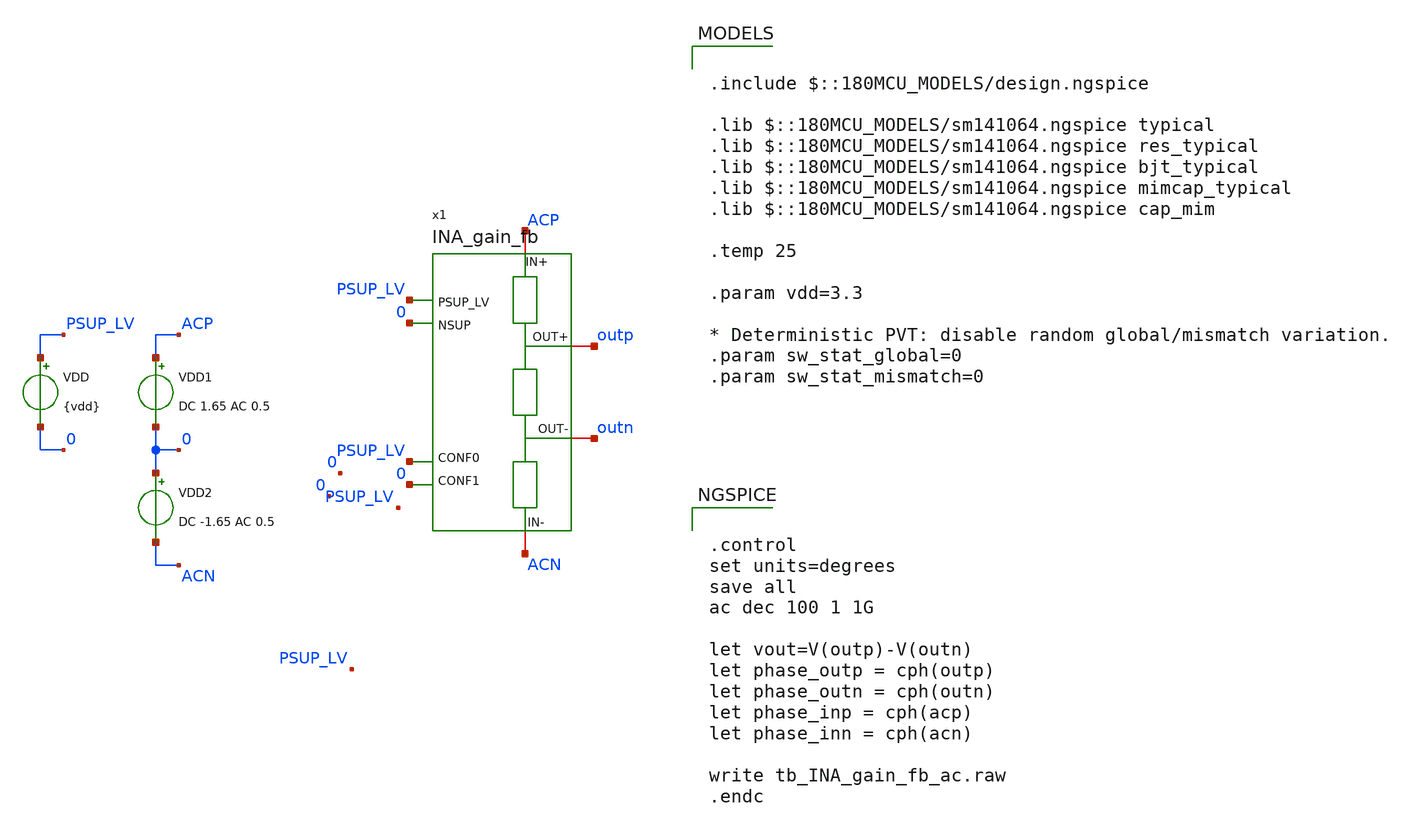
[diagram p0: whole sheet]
** sch_path: xschem/blocks/INA_gain_fb/tb_INA_gain_fb_ac.sch
**.subckt tb_INA_gain_fb_ac
VDD PSUP_LV 0 {vdd}
x1 ACP outp PSUP_LV 0 0 PSUP_LV outn ACN INA_gain_fb
VDD1 ACP 0 DC 1.65 AC 0.5
VDD2 0 ACN DC -1.65 AC 0.5
**** begin user architecture code

.include $::180MCU_MODELS/design.ngspice

.lib $::180MCU_MODELS/sm141064.ngspice typical
.lib $::180MCU_MODELS/sm141064.ngspice res_typical
.lib $::180MCU_MODELS/sm141064.ngspice bjt_typical
.lib $::180MCU_MODELS/sm141064.ngspice mimcap_typical
.lib $::180MCU_MODELS/sm141064.ngspice cap_mim

.temp 25

.param vdd=3.3

* Deterministic PVT: disable random global/mismatch variation.
.param sw_stat_global=0
.param sw_stat_mismatch=0



.control
set units=degrees
save all
ac dec 100 1 1G

let vout=V(outp)-V(outn)
let phase_outp = cph(outp)
let phase_outn = cph(outn)
let phase_inp = cph(acp)
let phase_inn = cph(acn)

write tb_INA_gain_fb_ac.raw
.endc


**** end user architecture code
**.ends

* expanding   symbol:  blocks/INA_gain_fb/INA_gain_fb.sym # of pins=8
** sym_path: xschem/blocks/INA_gain_fb/INA_gain_fb.sym
** sch_path: xschem/blocks/INA_gain_fb/INA_gain_fb.sch
.subckt INA_gain_fb IN+ OUT+ PSUP_LV NSUP CONF1 CONF0 OUT- IN-
*.iopin IN+
*.iopin IN-
*.iopin OUT-
*.iopin OUT+
*.ipin PSUP_LV
*.ipin NSUP
*.ipin CONF1
*.ipin CONF0
XR2 net1 net2 PSUP_LV ppolyf_u_1k r_width=1e-6 r_length=22e-6 m=1
XR4 net2 net3 PSUP_LV ppolyf_u_1k r_width=1e-6 r_length=220e-6 m=1
x1 C0 OUT+ net1 nC0 net7 net8 transmission_gate
x2 C1 OUT+ net2 nC1 net9 net10 transmission_gate
x7 C2 OUT+ net3 nC2 net11 net12 transmission_gate
x12 C3 OUT+ IN+ nC3 net13 net14 transmission_gate
XR9 net3 IN+ PSUP_LV ppolyf_u_1k r_width=1e-6 r_length=2200e-6 m=1
XR3 net4 net1 PSUP_LV ppolyf_u_1k r_width=1e-6 r_length=4.4e-6 m=1
XR6 net4 net5 PSUP_LV ppolyf_u_1k r_width=1e-6 r_length=22e-6 m=1
XR7 net5 net6 PSUP_LV ppolyf_u_1k r_width=1e-6 r_length=220e-6 m=1
XR14 net6 IN- PSUP_LV ppolyf_u_1k r_width=1e-6 r_length=2200e-6 m=1
x19 C0 OUT- net4 nC0 net15 net16 transmission_gate
x20 C1 OUT- net5 nC1 net17 net18 transmission_gate
x21 C2 OUT- net6 nC2 net19 net20 transmission_gate
x22 C3 OUT- IN- nC3 net21 net22 transmission_gate
x9 PSUP_LV nC1 C1 NSUP not
x10 PSUP_LV nC2 C2 NSUP not
x11 PSUP_LV nC3 C3 NSUP not
x31 PSUP_LV CONF0 nCONF0 NSUP not
x32 PSUP_LV CONF1 nCONF1 NSUP not
x35 PSUP_LV nC0 C0 NSUP not
x3 nC0 CONF0 CONF1 PSUP_LV NSUP nand_2
x4 nC1 nCONF0 CONF1 PSUP_LV NSUP nand_2
x5 nC2 CONF0 nCONF1 PSUP_LV NSUP nand_2
x6 nC3 nCONF0 nCONF1 PSUP_LV NSUP nand_2
.ends


* expanding   symbol:  blocks/transmission_gate/transmission_gate.sym # of pins=6
** sym_path: xschem/blocks/transmission_gate/transmission_gate.sym
** sch_path: xschem/blocks/transmission_gate/transmission_gate.sch
.subckt transmission_gate C A B nC VPOS VNEG
*.iopin A
*.iopin B
*.ipin C
*.ipin nC
*.ipin VPOS
*.ipin VNEG
XM3 A C B VNEG nfet_03v3 L=2u W=10u nf=1 ad='int((nf+1)/2) * W/nf * 0.18u' as='int((nf+2)/2) * W/nf * 0.18u'
+ pd='2*int((nf+1)/2) * (W/nf + 0.18u)' ps='2*int((nf+2)/2) * (W/nf + 0.18u)' nrd='0.18u / W' nrs='0.18u / W'
+ sa=0 sb=0 sd=0 m=2
XM4 A nC B VPOS pfet_03v3 L=2u W=10u nf=1 ad='int((nf+1)/2) * W/nf * 0.18u' as='int((nf+2)/2) * W/nf * 0.18u'
+ pd='2*int((nf+1)/2) * (W/nf + 0.18u)' ps='2*int((nf+2)/2) * (W/nf + 0.18u)' nrd='0.18u / W' nrs='0.18u / W'
+ sa=0 sb=0 sd=0 m=4
.ends


* expanding   symbol:  blocks/not/not.sym # of pins=6
** sym_path: xschem/blocks/not/not.sym
** sch_path: xschem/blocks/not/not.sch
.subckt not PSUP A B NSUP
*.ipin PSUP
*.ipin NSUP
*.ipin A
*.opin B
XM2 B A NSUP NSUP nfet_03v3 L=0.28u W=0.22u nf=1 ad='int((nf+1)/2) * W/nf * 0.18u' as='int((nf+2)/2) * W/nf * 0.18u'
+ pd='2*int((nf+1)/2) * (W/nf + 0.18u)' ps='2*int((nf+2)/2) * (W/nf + 0.18u)' nrd='0.18u / W' nrs='0.18u / W'
+ sa=0 sb=0 sd=0 m=1
XM1 B A PSUP PSUP pfet_03v3 L=0.28u W=0.5u nf=1 ad='int((nf+1)/2) * W/nf * 0.18u' as='int((nf+2)/2) * W/nf * 0.18u'
+ pd='2*int((nf+1)/2) * (W/nf + 0.18u)' ps='2*int((nf+2)/2) * (W/nf + 0.18u)' nrd='0.18u / W' nrs='0.18u / W'
+ sa=0 sb=0 sd=0 m=1
.ends


* expanding   symbol:  blocks/nand_2/nand_2.sym # of pins=7
** sym_path: xschem/blocks/nand_2/nand_2.sym
** sch_path: xschem/blocks/nand_2/nand_2.sch
.subckt nand_2 Y A B PSUP NSUP
*.ipin PSUP
*.ipin NSUP
*.ipin A
*.ipin B
*.opin Y
XM5 net1 B NSUP NSUP nfet_03v3 L=0.28u W=0.22u nf=1 ad='int((nf+1)/2) * W/nf * 0.18u' as='int((nf+2)/2) * W/nf * 0.18u'
+ pd='2*int((nf+1)/2) * (W/nf + 0.18u)' ps='2*int((nf+2)/2) * (W/nf + 0.18u)' nrd='0.18u / W' nrs='0.18u / W'
+ sa=0 sb=0 sd=0 m=1
XM1 Y A net1 NSUP nfet_03v3 L=0.28u W=0.22u nf=1 ad='int((nf+1)/2) * W/nf * 0.18u' as='int((nf+2)/2) * W/nf * 0.18u'
+ pd='2*int((nf+1)/2) * (W/nf + 0.18u)' ps='2*int((nf+2)/2) * (W/nf + 0.18u)' nrd='0.18u / W' nrs='0.18u / W'
+ sa=0 sb=0 sd=0 m=1
XM2 Y A PSUP PSUP pfet_03v3 L=0.28u W=0.5u nf=1 ad='int((nf+1)/2) * W/nf * 0.18u' as='int((nf+2)/2) * W/nf * 0.18u'
+ pd='2*int((nf+1)/2) * (W/nf + 0.18u)' ps='2*int((nf+2)/2) * (W/nf + 0.18u)' nrd='0.18u / W' nrs='0.18u / W'
+ sa=0 sb=0 sd=0 m=1
XM3 Y B PSUP PSUP pfet_03v3 L=0.28u W=0.5u nf=1 ad='int((nf+1)/2) * W/nf * 0.18u' as='int((nf+2)/2) * W/nf * 0.18u'
+ pd='2*int((nf+1)/2) * (W/nf + 0.18u)' ps='2*int((nf+2)/2) * (W/nf + 0.18u)' nrd='0.18u / W' nrs='0.18u / W'
+ sa=0 sb=0 sd=0 m=1
.ends

.end
